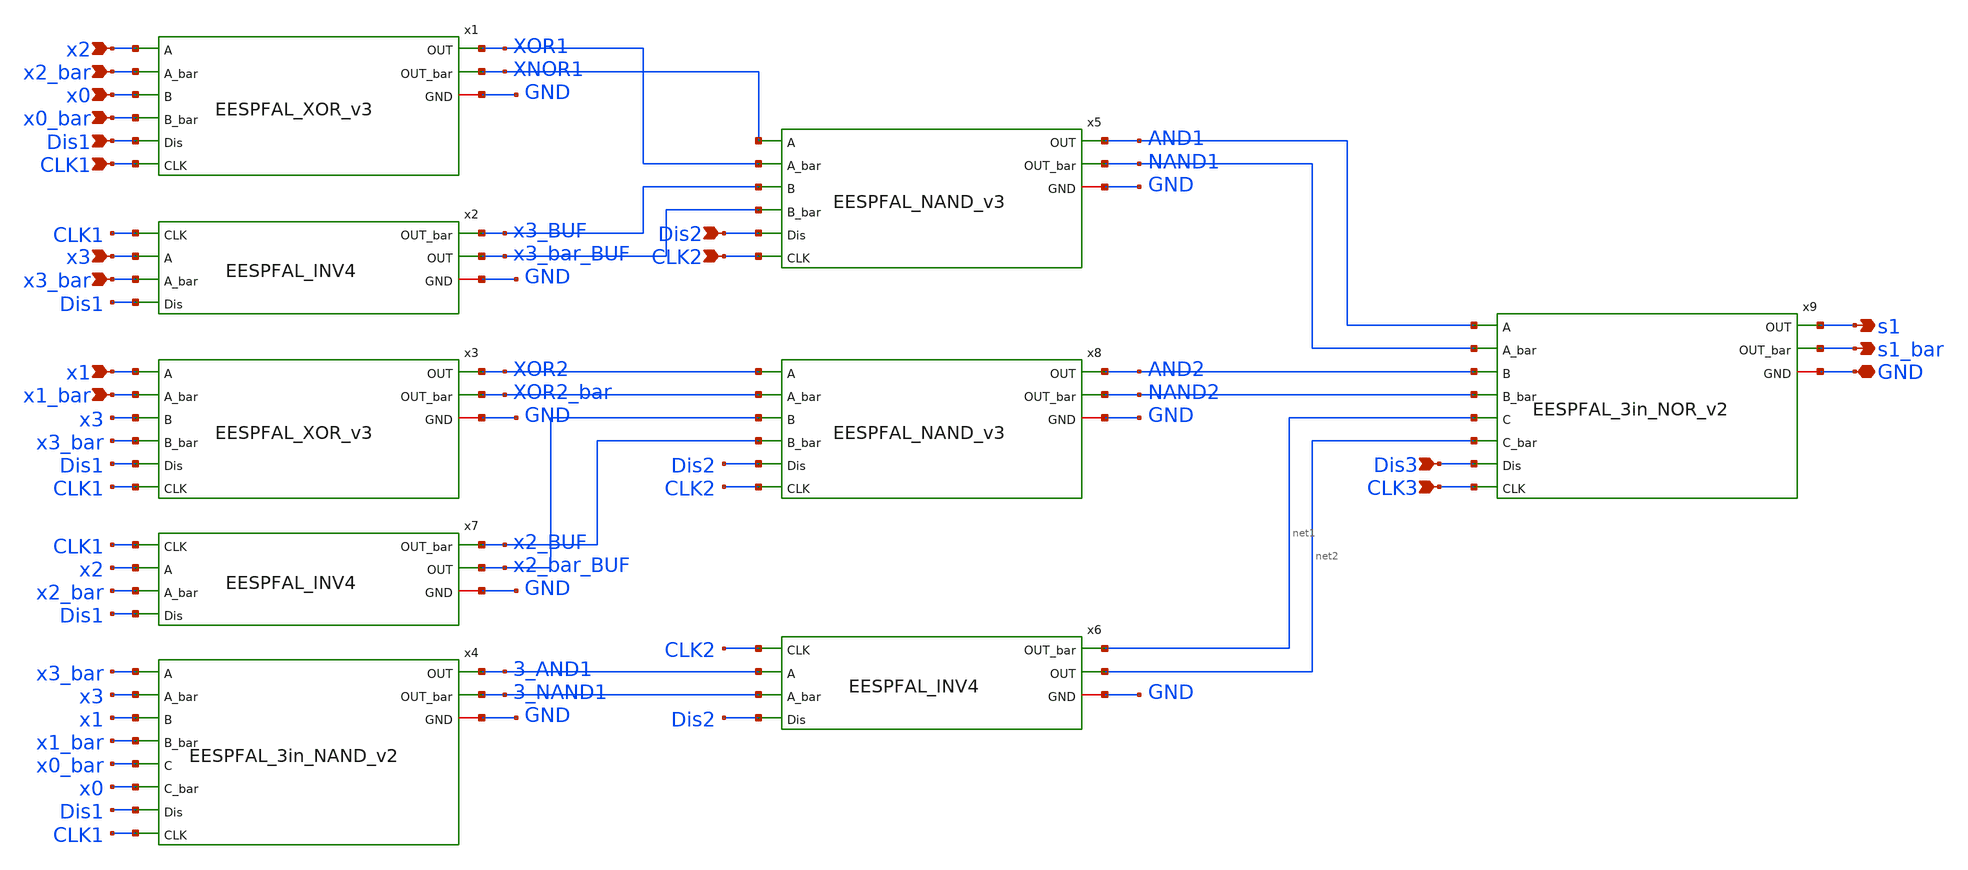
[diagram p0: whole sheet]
** sch_path: skywater_stuff/EESPFAL_s1_magic_checked.sch
**.subckt EESPFAL_s1_magic_checked x0 x0_bar x1 x1_bar x2 x2_bar x3 x3_bar s1 s1_bar Dis1 Dis2 Dis3
*+ CLK1 CLK2 CLK3 GND
*.ipin x0
*.ipin x0_bar
*.ipin x1
*.ipin x1_bar
*.ipin x2
*.ipin x2_bar
*.ipin x3
*.ipin x3_bar
*.opin s1
*.opin s1_bar
*.ipin Dis1
*.ipin Dis2
*.ipin Dis3
*.ipin CLK1
*.ipin CLK2
*.ipin CLK3
*.iopin GND
x4 x3_bar x3 x1 x1_bar x0_bar x0 3_AND1 3_NAND1 Dis1 GND CLK1 EESPFAL_3in_NAND_v2
x5 XNOR1 XOR1 x3_BUF x3_bar_BUF AND1 NAND1 Dis2 GND CLK2 EESPFAL_NAND_v3
x6 3_AND1 3_NAND1 net2 net1 Dis2 GND CLK2 EESPFAL_INV4
x8 XOR2 XOR2_bar x2_bar_BUF x2_BUF AND2 NAND2 Dis2 GND CLK2 EESPFAL_NAND_v3
x9 AND1 NAND1 AND2 NAND2 net1 net2 s1 s1_bar Dis3 GND CLK3 EESPFAL_3in_NOR_v2
x7 x2 x2_bar x2_bar_BUF x2_BUF Dis1 GND CLK1 EESPFAL_INV4
x1 x2 x2_bar x0 x0_bar XOR1 XNOR1 Dis1 GND CLK1 EESPFAL_XOR_v3
x2 x3 x3_bar x3_bar_BUF x3_BUF Dis1 GND CLK1 EESPFAL_INV4
x3 x1 x1_bar x3 x3_bar XOR2 XOR2_bar Dis1 GND CLK1 EESPFAL_XOR_v3
**.ends
.end
